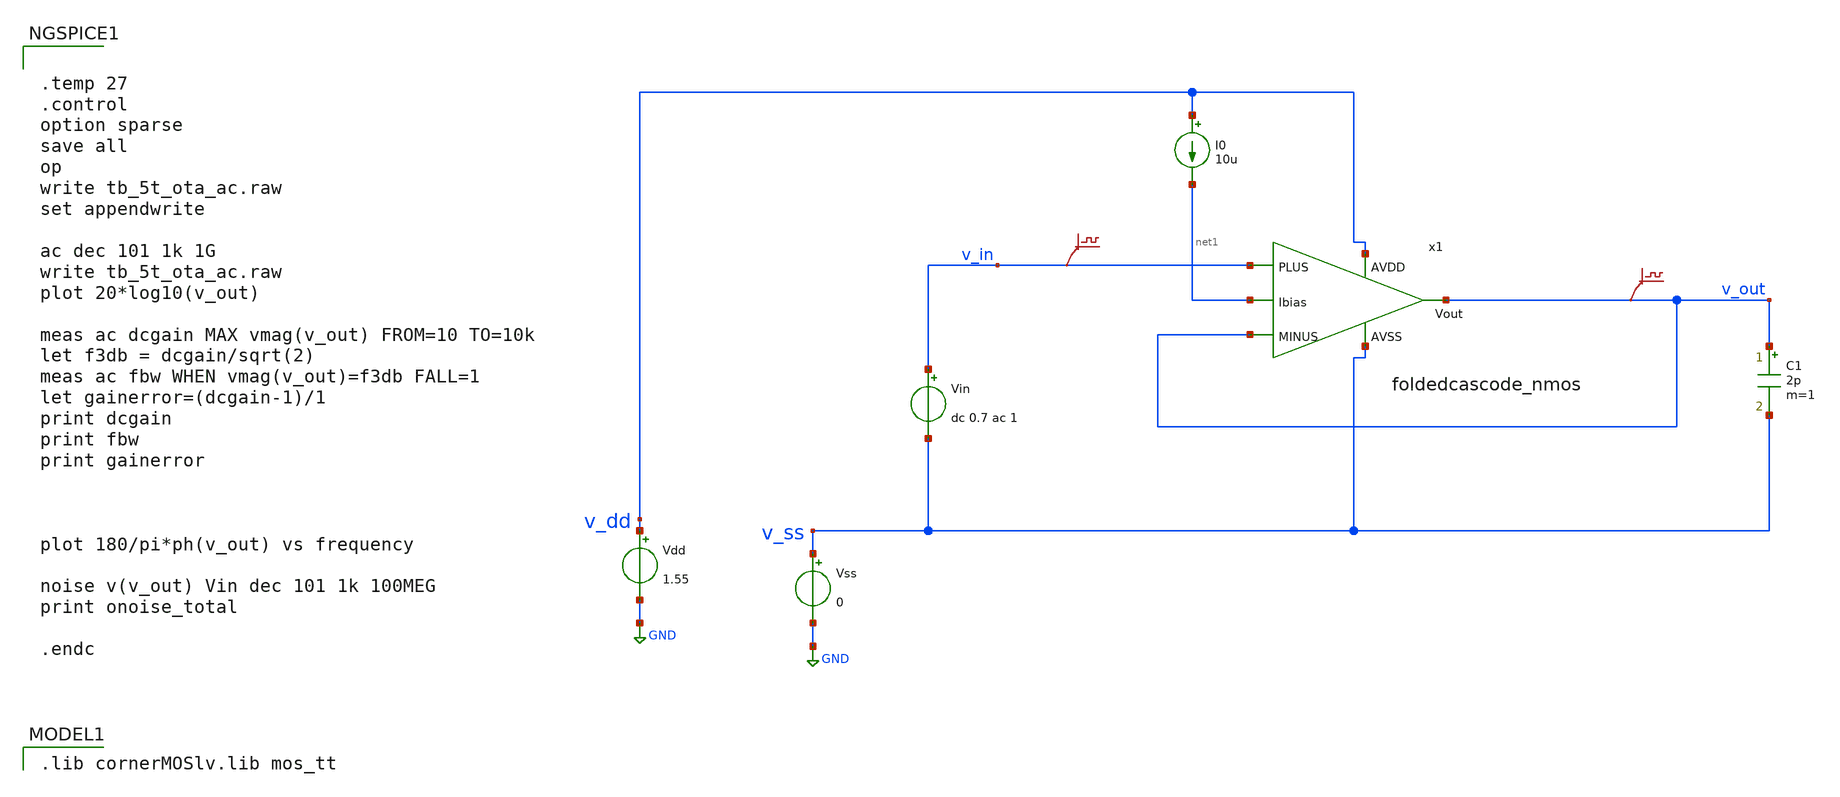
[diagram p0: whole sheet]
** sch_path: Designs/otas/tb_foldedcascode_n_ac.sch
**.subckt tb_foldedcascode_n_ac
Vss v_ss GND 0
Vdd v_dd GND 1.55
Vin v_in v_ss dc 0.7 ac 1
.save v(v_in)
I0 v_dd net1 10u
C1 v_out v_ss 2p m=1
.save v(v_out)
x1 v_dd v_in v_out v_out net1 v_ss foldedcascode_nmos
**** begin user architecture code
 .lib cornerMOSlv.lib mos_tt



.temp 27
.control
option sparse
save all
op
write tb_5t_ota_ac.raw
set appendwrite

ac dec 101 1k 1G
write tb_5t_ota_ac.raw
plot 20*log10(v_out)

meas ac dcgain MAX vmag(v_out) FROM=10 TO=10k
let f3db = dcgain/sqrt(2)
meas ac fbw WHEN vmag(v_out)=f3db FALL=1
let gainerror=(dcgain-1)/1
print dcgain
print fbw
print gainerror



plot 180/pi*ph(v_out) vs frequency

noise v(v_out) Vin dec 101 1k 100MEG
print onoise_total

.endc


**** end user architecture code
**.ends

* expanding   symbol:  foldedcascode_nmos.sym # of pins=6
** sym_path: Designs/otas/foldedcascode_nmos.sym
** sch_path: Designs/otas/foldedcascode_nmos.sch
.subckt foldedcascode_nmos AVDD PLUS MINUS Vout Ibias AVSS
*.ipin PLUS
*.ipin MINUS
*.opin Vout
*.ipin AVDD
*.ipin AVSS
*.ipin Ibias
XM6 net5 PLUS net1 AVSS sg13_lv_nmos w=5u l=1u ng=1 m=1 mm_ok=1
XM8 net1 Ibias AVSS AVSS sg13_lv_nmos w=25u l=5u ng=3 m=1 mm_ok=1
XM21 net3 net4 AVSS AVSS sg13_lv_nmos w=1u l=0.5u ng=1 m=1 mm_ok=1
XM22 net2 net4 AVSS AVSS sg13_lv_nmos w=1u l=0.5u ng=1 m=1 mm_ok=1
XM7 net6 MINUS net1 AVSS sg13_lv_nmos w=5u l=1u ng=1 m=1 mm_ok=1
XM23 net4 net9 net2 AVSS sg13_lv_nmos w=1.5u l=0.5u ng=1 m=1 mm_ok=1
XM24 Vout net9 net3 AVSS sg13_lv_nmos w=1.5u l=0.5u ng=1 m=1 mm_ok=1
XM25 net4 net8 net5 AVDD sg13_lv_pmos w=6u l=0.5u ng=1 m=1 mm_ok=1
XM26 net5 net7 AVDD AVDD sg13_lv_pmos w=6u l=0.5u ng=1 m=1 mm_ok=1
XM27 Vout net8 net6 AVDD sg13_lv_pmos w=6u l=0.5u ng=1 m=1 mm_ok=1
XM28 net6 net7 AVDD AVDD sg13_lv_pmos w=6u l=0.5u ng=1 m=1 mm_ok=1
XM1 Ibias Ibias AVSS AVSS sg13_lv_nmos w=18u l=5u ng=2 m=1 mm_ok=1
XM2 net8 net8 net7 AVDD sg13_lv_pmos w=6u l=0.5u ng=2 m=1 mm_ok=1
XM3 net7 net7 AVDD AVDD sg13_lv_pmos w=6u l=0.5u ng=2 m=1 mm_ok=1
XM4 net9 net7 AVDD AVDD sg13_lv_pmos w=6u l=0.5u ng=2 m=1 mm_ok=1
XM5 net9 net9 AVSS AVSS sg13_lv_nmos w=1.5u l=0.5u ng=1 m=1 mm_ok=1
XM9 net8 Ibias AVSS AVSS sg13_lv_nmos w=25u l=5u ng=3 m=1 mm_ok=1
.ends

.GLOBAL GND
.end
